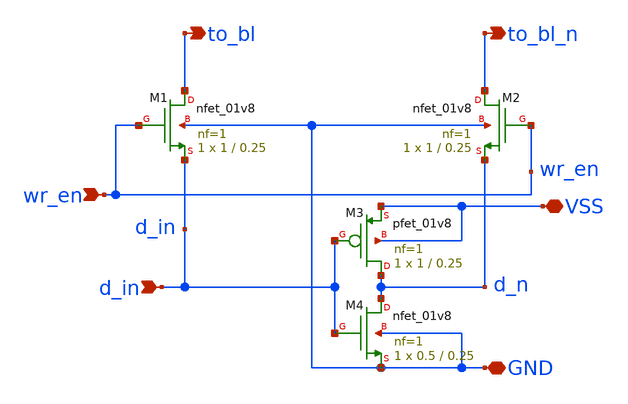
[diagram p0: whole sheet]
** sch_path: write_driver.sch
**.subckt write_driver d_in wr_en to_bl to_bl_n VSS GND
*.ipin d_in
*.ipin wr_en
*.opin to_bl
*.opin to_bl_n
*.iopin VSS
*.iopin GND
XM1 to_bl wr_en d_in GND sky130_fd_pr__nfet_01v8 L=0.25 W=1 nf=1 ad='int((nf+1)/2) * W/nf * 0.29' as='int((nf+2)/2) * W/nf * 0.29'
+ pd='2*int((nf+1)/2) * (W/nf + 0.29)' ps='2*int((nf+2)/2) * (W/nf + 0.29)' nrd='0.29 / W' nrs='0.29 / W'
+ sa=0 sb=0 sd=0 mult=1 m=1
XM2 to_bl_n wr_en d_n GND sky130_fd_pr__nfet_01v8 L=0.25 W=1 nf=1 ad='int((nf+1)/2) * W/nf * 0.29' as='int((nf+2)/2) * W/nf * 0.29'
+ pd='2*int((nf+1)/2) * (W/nf + 0.29)' ps='2*int((nf+2)/2) * (W/nf + 0.29)' nrd='0.29 / W' nrs='0.29 / W'
+ sa=0 sb=0 sd=0 mult=1 m=1
XM3 d_n d_in VSS VSS sky130_fd_pr__pfet_01v8 L=0.25 W=1 nf=1 ad='int((nf+1)/2) * W/nf * 0.29' as='int((nf+2)/2) * W/nf * 0.29'
+ pd='2*int((nf+1)/2) * (W/nf + 0.29)' ps='2*int((nf+2)/2) * (W/nf + 0.29)' nrd='0.29 / W' nrs='0.29 / W'
+ sa=0 sb=0 sd=0 mult=1 m=1
XM4 d_n d_in GND GND sky130_fd_pr__nfet_01v8 L=0.25 W=0.5 nf=1 ad='int((nf+1)/2) * W/nf * 0.29' as='int((nf+2)/2) * W/nf * 0.29'
+ pd='2*int((nf+1)/2) * (W/nf + 0.29)' ps='2*int((nf+2)/2) * (W/nf + 0.29)' nrd='0.29 / W' nrs='0.29 / W'
+ sa=0 sb=0 sd=0 mult=1 m=1
**.ends
.end
